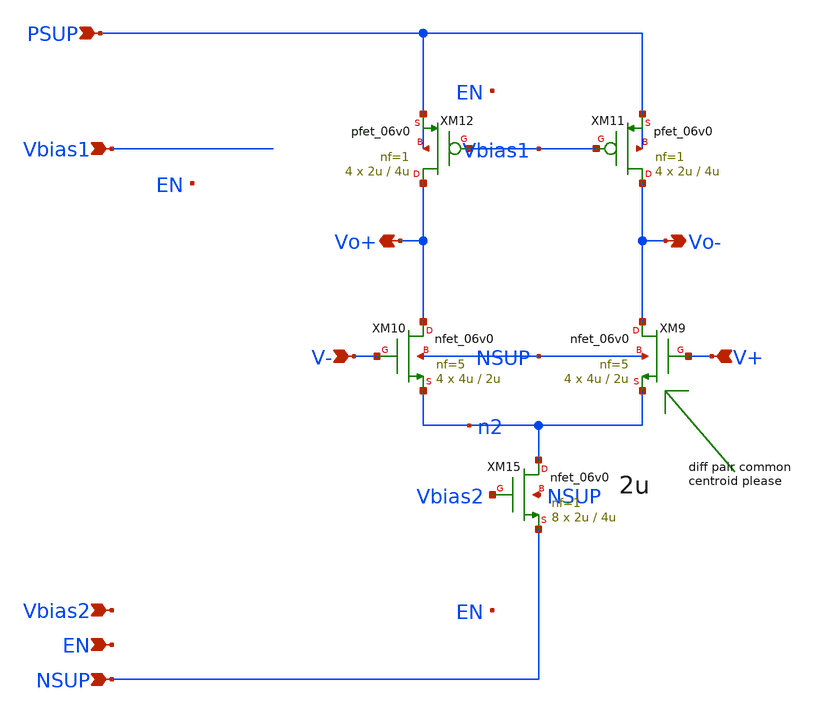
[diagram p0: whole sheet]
** sch_path: xschem/blocks/aux_amp_gb/aux_amp_gb.sch
**.subckt aux_amp_gb PSUP NSUP EN Vo- V+ V- Vo+ Vbias1 Vbias2
*.ipin PSUP
*.ipin NSUP
*.ipin EN
*.opin Vo-
*.ipin V+
*.ipin V-
*.opin Vo+
*.ipin Vbias1
*.ipin Vbias2
XM9 Vo- V+ n2 NSUP nfet_06v0 L=2u W=4u nf=5 ad='int((nf+1)/2) * W/nf * 0.18u' as='int((nf+2)/2) * W/nf * 0.18u'
+ pd='2*int((nf+1)/2) * (W/nf + 0.18u)' ps='2*int((nf+2)/2) * (W/nf + 0.18u)' nrd='0.18u / W' nrs='0.18u / W'
+ sa=0 sb=0 sd=0 m=4
XM10 Vo+ V- n2 NSUP nfet_06v0 L=2u W=4u nf=5 ad='int((nf+1)/2) * W/nf * 0.18u' as='int((nf+2)/2) * W/nf * 0.18u'
+ pd='2*int((nf+1)/2) * (W/nf + 0.18u)' ps='2*int((nf+2)/2) * (W/nf + 0.18u)' nrd='0.18u / W' nrs='0.18u / W'
+ sa=0 sb=0 sd=0 m=4
XM11 Vo- Vbias1 PSUP PSUP pfet_06v0 L=4u W=2u nf=1 ad='int((nf+1)/2) * W/nf * 0.18u' as='int((nf+2)/2) * W/nf * 0.18u'
+ pd='2*int((nf+1)/2) * (W/nf + 0.18u)' ps='2*int((nf+2)/2) * (W/nf + 0.18u)' nrd='0.18u / W' nrs='0.18u / W'
+ sa=0 sb=0 sd=0 m=4
XM12 Vo+ Vbias1 PSUP PSUP pfet_06v0 L=4u W=2u nf=1 ad='int((nf+1)/2) * W/nf * 0.18u' as='int((nf+2)/2) * W/nf * 0.18u'
+ pd='2*int((nf+1)/2) * (W/nf + 0.18u)' ps='2*int((nf+2)/2) * (W/nf + 0.18u)' nrd='0.18u / W' nrs='0.18u / W'
+ sa=0 sb=0 sd=0 m=4
XM15 n2 Vbias2 NSUP NSUP nfet_06v0 L=4u W=2u nf=1 ad='int((nf+1)/2) * W/nf * 0.18u' as='int((nf+2)/2) * W/nf * 0.18u'
+ pd='2*int((nf+1)/2) * (W/nf + 0.18u)' ps='2*int((nf+2)/2) * (W/nf + 0.18u)' nrd='0.18u / W' nrs='0.18u / W'
+ sa=0 sb=0 sd=0 m=8
**.ends
.end
